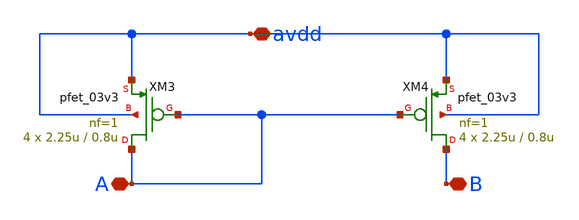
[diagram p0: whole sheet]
** sch_path: LDO/xschem/isource/cm.sch
**.subckt cm avdd A B
*.iopin avdd
*.iopin A
*.iopin B
XM3 A A avdd avdd pfet_03v3 L=0.8u W=2.25u nf=1 ad='int((nf+1)/2) * W/nf * 0.18u' as='int((nf+2)/2) * W/nf * 0.18u'
+ pd='2*int((nf+1)/2) * (W/nf + 0.18u)' ps='2*int((nf+2)/2) * (W/nf + 0.18u)' nrd='0.18u / W' nrs='0.18u / W'
+ sa=0 sb=0 sd=0 m=4
XM4 B A avdd avdd pfet_03v3 L=0.8u W=2.25u nf=1 ad='int((nf+1)/2) * W/nf * 0.18u' as='int((nf+2)/2) * W/nf * 0.18u'
+ pd='2*int((nf+1)/2) * (W/nf + 0.18u)' ps='2*int((nf+2)/2) * (W/nf + 0.18u)' nrd='0.18u / W' nrs='0.18u / W'
+ sa=0 sb=0 sd=0 m=4
**.ends
.end
